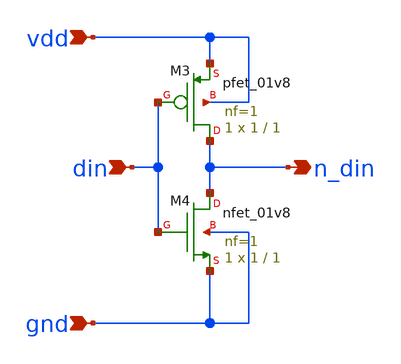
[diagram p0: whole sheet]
** sch_path: Symbols/inverter.sch
**.subckt inverter gnd n_din din vdd
*.ipin gnd
*.opin n_din
*.ipin din
*.ipin vdd
XM3 n_din din vdd vdd sky130_fd_pr__pfet_01v8 L=1 W=1 nf=1 ad='int((nf+1)/2) * W/nf * 0.29' as='int((nf+2)/2) * W/nf * 0.29'
+ pd='2*int((nf+1)/2) * (W/nf + 0.29)' ps='2*int((nf+2)/2) * (W/nf + 0.29)' nrd='0.29 / W' nrs='0.29 / W'
+ sa=0 sb=0 sd=0 mult=1 m=1
XM4 n_din din gnd gnd sky130_fd_pr__nfet_01v8 L=1 W=1 nf=1 ad='int((1 + 1)/2) * 1 / 1 * 0.29' as='int((1 + 2)/2) * 1 / 1 * 0.29'
+ pd='2*int((1 + 1)/2) * (1 / 1 + 0.29)' ps='2*int((1 + 2)/2) * (1 / 1 + 0.29)' nrd='0.29 / 1 ' nrs='0.29 / 1 '
+ sa=0 sb=0 sd=0 mult=1 m=1
**.ends
.end
